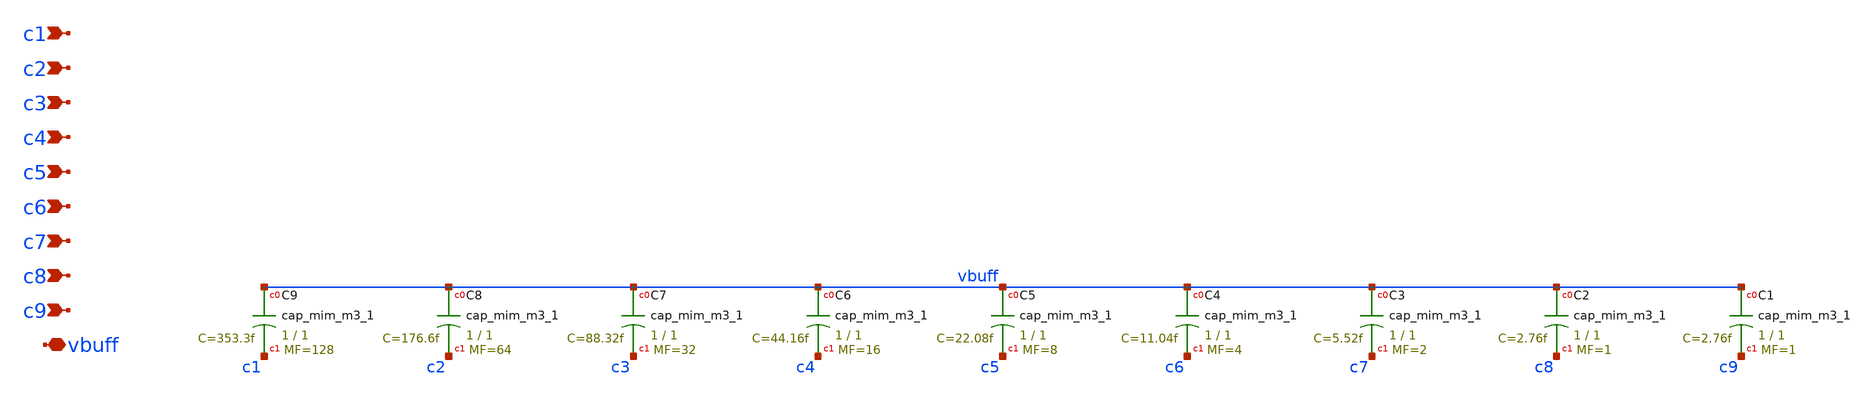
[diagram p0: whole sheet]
** sch_path: xschem/cap_array.sch
**.subckt cap_array c1 c2 c3 c4 c5 c6 c7 c8 c9 vbuff
*.ipin c1
*.ipin c2
*.ipin c3
*.ipin c4
*.ipin c5
*.ipin c6
*.ipin c7
*.ipin c8
*.ipin c9
*.iopin vbuff
XC1 vbuff c9 sky130_fd_pr__cap_mim_m3_1 W=1 L=1 MF=1 m=1
XC2 vbuff c8 sky130_fd_pr__cap_mim_m3_1 W=1 L=1 MF=1 m=1
XC3 vbuff c7 sky130_fd_pr__cap_mim_m3_1 W=1 L=1 MF=2 m=2
XC4 vbuff c6 sky130_fd_pr__cap_mim_m3_1 W=1 L=1 MF=4 m=4
XC5 vbuff c5 sky130_fd_pr__cap_mim_m3_1 W=1 L=1 MF=8 m=8
XC6 vbuff c4 sky130_fd_pr__cap_mim_m3_1 W=1 L=1 MF=16 m=16
XC7 vbuff c3 sky130_fd_pr__cap_mim_m3_1 W=1 L=1 MF=32 m=32
XC8 vbuff c2 sky130_fd_pr__cap_mim_m3_1 W=1 L=1 MF=64 m=64
XC9 vbuff c1 sky130_fd_pr__cap_mim_m3_1 W=1 L=1 MF=128 m=128
**.ends
.end
